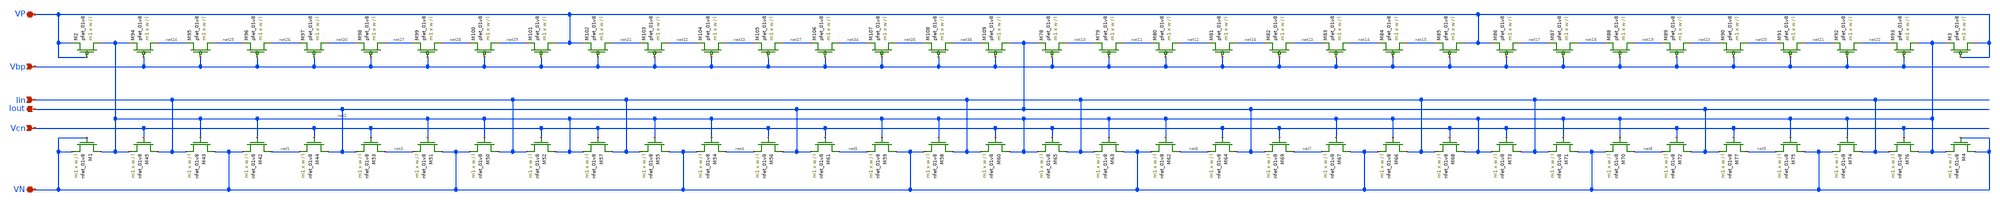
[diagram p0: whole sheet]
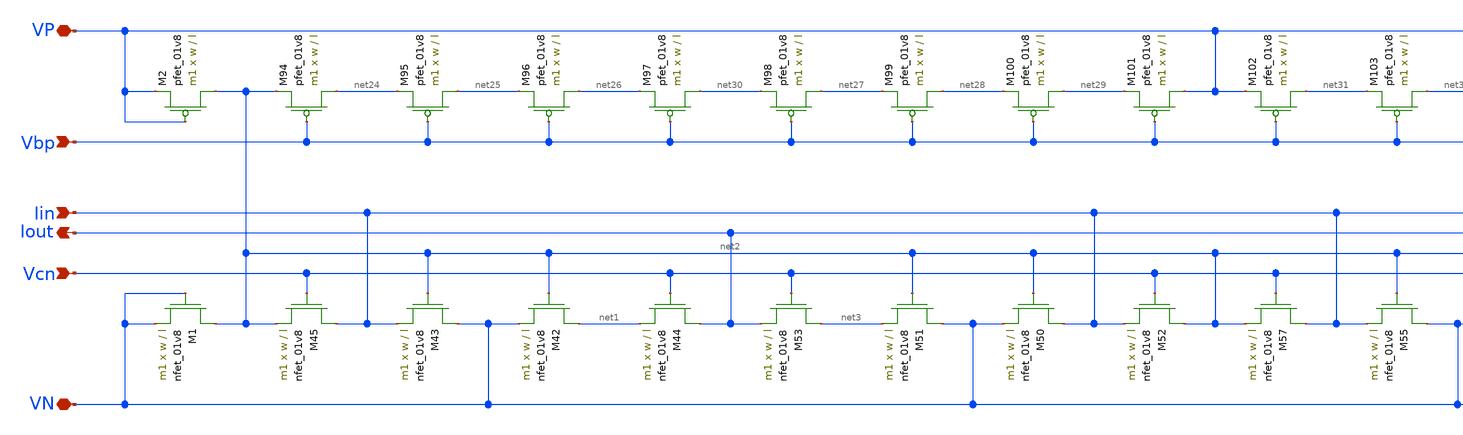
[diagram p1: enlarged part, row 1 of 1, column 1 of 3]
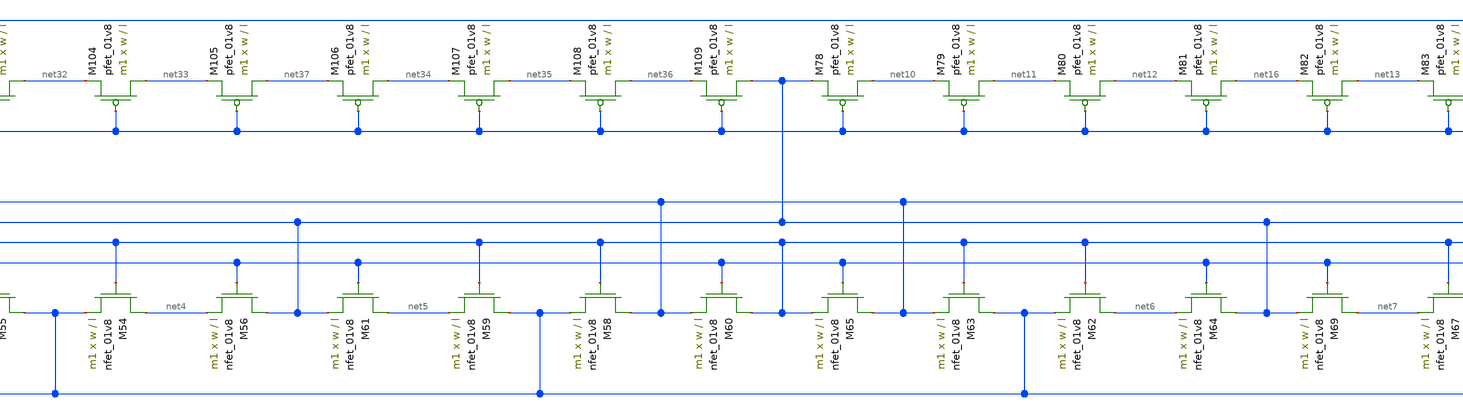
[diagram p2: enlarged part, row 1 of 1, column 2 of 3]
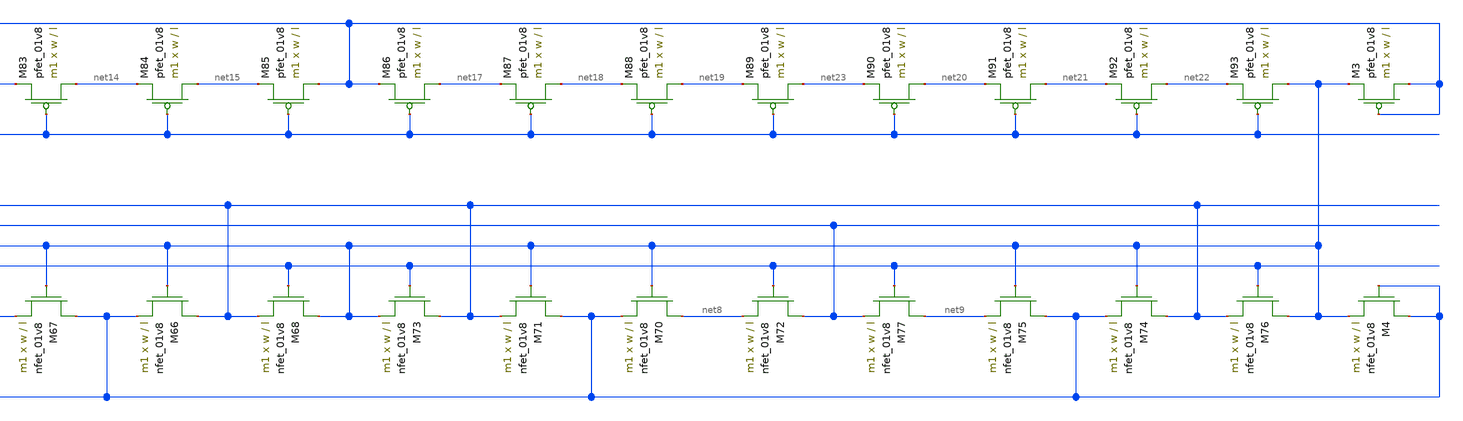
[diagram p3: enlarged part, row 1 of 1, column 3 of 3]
** sch_path: schematic/old/iout_mirror_LDS.sch
**.subckt iout_mirror_LDS Vcn Vbp Iout Iin VN VP
*.ipin Vcn
*.ipin Vbp
*.opin Iout
*.ipin Iin
*.iopin VN
*.iopin VP
XM42 net1 net2 VN GND sky130_fd_pr__nfet_01v8 L=l W=w nf=1 ad='int((nf+1)/2) * W/nf * 0.29' as='int((nf+2)/2) * W/nf * 0.29'
+ pd='2*int((nf+1)/2) * (W/nf + 0.29)' ps='2*int((nf+2)/2) * (W/nf + 0.29)' nrd='0.29 / W' nrs='0.29 / W'
+ sa=0 sb=0 sd=0 mult=m1 m=m1
XM43 VN net2 Iin GND sky130_fd_pr__nfet_01v8 L=l W=w nf=1 ad='int((nf+1)/2) * W/nf * 0.29' as='int((nf+2)/2) * W/nf * 0.29'
+ pd='2*int((nf+1)/2) * (W/nf + 0.29)' ps='2*int((nf+2)/2) * (W/nf + 0.29)' nrd='0.29 / W' nrs='0.29 / W'
+ sa=0 sb=0 sd=0 mult=m1 m=m1
XM44 Iout Vcn net1 GND sky130_fd_pr__nfet_01v8 L=l W=w nf=1 ad='int((nf+1)/2) * W/nf * 0.29' as='int((nf+2)/2) * W/nf * 0.29'
+ pd='2*int((nf+1)/2) * (W/nf + 0.29)' ps='2*int((nf+2)/2) * (W/nf + 0.29)' nrd='0.29 / W' nrs='0.29 / W'
+ sa=0 sb=0 sd=0 mult=m1 m=m1
XM45 Iin Vcn net2 GND sky130_fd_pr__nfet_01v8 L=l W=w nf=1 ad='int((nf+1)/2) * W/nf * 0.29' as='int((nf+2)/2) * W/nf * 0.29'
+ pd='2*int((nf+1)/2) * (W/nf + 0.29)' ps='2*int((nf+2)/2) * (W/nf + 0.29)' nrd='0.29 / W' nrs='0.29 / W'
+ sa=0 sb=0 sd=0 mult=m1 m=m1
XM50 Iin net2 VN GND sky130_fd_pr__nfet_01v8 L=l W=w nf=1 ad='int((nf+1)/2) * W/nf * 0.29' as='int((nf+2)/2) * W/nf * 0.29'
+ pd='2*int((nf+1)/2) * (W/nf + 0.29)' ps='2*int((nf+2)/2) * (W/nf + 0.29)' nrd='0.29 / W' nrs='0.29 / W'
+ sa=0 sb=0 sd=0 mult=m1 m=m1
XM51 VN net2 net3 GND sky130_fd_pr__nfet_01v8 L=l W=w nf=1 ad='int((nf+1)/2) * W/nf * 0.29' as='int((nf+2)/2) * W/nf * 0.29'
+ pd='2*int((nf+1)/2) * (W/nf + 0.29)' ps='2*int((nf+2)/2) * (W/nf + 0.29)' nrd='0.29 / W' nrs='0.29 / W'
+ sa=0 sb=0 sd=0 mult=m1 m=m1
XM52 net2 Vcn Iin GND sky130_fd_pr__nfet_01v8 L=l W=w nf=1 ad='int((nf+1)/2) * W/nf * 0.29' as='int((nf+2)/2) * W/nf * 0.29'
+ pd='2*int((nf+1)/2) * (W/nf + 0.29)' ps='2*int((nf+2)/2) * (W/nf + 0.29)' nrd='0.29 / W' nrs='0.29 / W'
+ sa=0 sb=0 sd=0 mult=m1 m=m1
XM53 net3 Vcn Iout GND sky130_fd_pr__nfet_01v8 L=l W=w nf=1 ad='int((nf+1)/2) * W/nf * 0.29' as='int((nf+2)/2) * W/nf * 0.29'
+ pd='2*int((nf+1)/2) * (W/nf + 0.29)' ps='2*int((nf+2)/2) * (W/nf + 0.29)' nrd='0.29 / W' nrs='0.29 / W'
+ sa=0 sb=0 sd=0 mult=m1 m=m1
XM54 net4 net2 VN GND sky130_fd_pr__nfet_01v8 L=l W=w nf=1 ad='int((nf+1)/2) * W/nf * 0.29' as='int((nf+2)/2) * W/nf * 0.29'
+ pd='2*int((nf+1)/2) * (W/nf + 0.29)' ps='2*int((nf+2)/2) * (W/nf + 0.29)' nrd='0.29 / W' nrs='0.29 / W'
+ sa=0 sb=0 sd=0 mult=m1 m=m1
XM55 VN net2 Iin GND sky130_fd_pr__nfet_01v8 L=l W=w nf=1 ad='int((nf+1)/2) * W/nf * 0.29' as='int((nf+2)/2) * W/nf * 0.29'
+ pd='2*int((nf+1)/2) * (W/nf + 0.29)' ps='2*int((nf+2)/2) * (W/nf + 0.29)' nrd='0.29 / W' nrs='0.29 / W'
+ sa=0 sb=0 sd=0 mult=m1 m=m1
XM56 Iout Vcn net4 GND sky130_fd_pr__nfet_01v8 L=l W=w nf=1 ad='int((nf+1)/2) * W/nf * 0.29' as='int((nf+2)/2) * W/nf * 0.29'
+ pd='2*int((nf+1)/2) * (W/nf + 0.29)' ps='2*int((nf+2)/2) * (W/nf + 0.29)' nrd='0.29 / W' nrs='0.29 / W'
+ sa=0 sb=0 sd=0 mult=m1 m=m1
XM57 Iin Vcn net2 GND sky130_fd_pr__nfet_01v8 L=l W=w nf=1 ad='int((nf+1)/2) * W/nf * 0.29' as='int((nf+2)/2) * W/nf * 0.29'
+ pd='2*int((nf+1)/2) * (W/nf + 0.29)' ps='2*int((nf+2)/2) * (W/nf + 0.29)' nrd='0.29 / W' nrs='0.29 / W'
+ sa=0 sb=0 sd=0 mult=m1 m=m1
XM58 Iin net2 VN GND sky130_fd_pr__nfet_01v8 L=l W=w nf=1 ad='int((nf+1)/2) * W/nf * 0.29' as='int((nf+2)/2) * W/nf * 0.29'
+ pd='2*int((nf+1)/2) * (W/nf + 0.29)' ps='2*int((nf+2)/2) * (W/nf + 0.29)' nrd='0.29 / W' nrs='0.29 / W'
+ sa=0 sb=0 sd=0 mult=m1 m=m1
XM59 VN net2 net5 GND sky130_fd_pr__nfet_01v8 L=l W=w nf=1 ad='int((nf+1)/2) * W/nf * 0.29' as='int((nf+2)/2) * W/nf * 0.29'
+ pd='2*int((nf+1)/2) * (W/nf + 0.29)' ps='2*int((nf+2)/2) * (W/nf + 0.29)' nrd='0.29 / W' nrs='0.29 / W'
+ sa=0 sb=0 sd=0 mult=m1 m=m1
XM60 net2 Vcn Iin GND sky130_fd_pr__nfet_01v8 L=l W=w nf=1 ad='int((nf+1)/2) * W/nf * 0.29' as='int((nf+2)/2) * W/nf * 0.29'
+ pd='2*int((nf+1)/2) * (W/nf + 0.29)' ps='2*int((nf+2)/2) * (W/nf + 0.29)' nrd='0.29 / W' nrs='0.29 / W'
+ sa=0 sb=0 sd=0 mult=m1 m=m1
XM61 net5 Vcn Iout GND sky130_fd_pr__nfet_01v8 L=l W=w nf=1 ad='int((nf+1)/2) * W/nf * 0.29' as='int((nf+2)/2) * W/nf * 0.29'
+ pd='2*int((nf+1)/2) * (W/nf + 0.29)' ps='2*int((nf+2)/2) * (W/nf + 0.29)' nrd='0.29 / W' nrs='0.29 / W'
+ sa=0 sb=0 sd=0 mult=m1 m=m1
XM62 net6 net2 VN GND sky130_fd_pr__nfet_01v8 L=l W=w nf=1 ad='int((nf+1)/2) * W/nf * 0.29' as='int((nf+2)/2) * W/nf * 0.29'
+ pd='2*int((nf+1)/2) * (W/nf + 0.29)' ps='2*int((nf+2)/2) * (W/nf + 0.29)' nrd='0.29 / W' nrs='0.29 / W'
+ sa=0 sb=0 sd=0 mult=m1 m=m1
XM63 VN net2 Iin GND sky130_fd_pr__nfet_01v8 L=l W=w nf=1 ad='int((nf+1)/2) * W/nf * 0.29' as='int((nf+2)/2) * W/nf * 0.29'
+ pd='2*int((nf+1)/2) * (W/nf + 0.29)' ps='2*int((nf+2)/2) * (W/nf + 0.29)' nrd='0.29 / W' nrs='0.29 / W'
+ sa=0 sb=0 sd=0 mult=m1 m=m1
XM64 Iout Vcn net6 GND sky130_fd_pr__nfet_01v8 L=l W=w nf=1 ad='int((nf+1)/2) * W/nf * 0.29' as='int((nf+2)/2) * W/nf * 0.29'
+ pd='2*int((nf+1)/2) * (W/nf + 0.29)' ps='2*int((nf+2)/2) * (W/nf + 0.29)' nrd='0.29 / W' nrs='0.29 / W'
+ sa=0 sb=0 sd=0 mult=m1 m=m1
XM65 Iin Vcn net2 GND sky130_fd_pr__nfet_01v8 L=l W=w nf=1 ad='int((nf+1)/2) * W/nf * 0.29' as='int((nf+2)/2) * W/nf * 0.29'
+ pd='2*int((nf+1)/2) * (W/nf + 0.29)' ps='2*int((nf+2)/2) * (W/nf + 0.29)' nrd='0.29 / W' nrs='0.29 / W'
+ sa=0 sb=0 sd=0 mult=m1 m=m1
XM66 Iin net2 VN GND sky130_fd_pr__nfet_01v8 L=l W=w nf=1 ad='int((nf+1)/2) * W/nf * 0.29' as='int((nf+2)/2) * W/nf * 0.29'
+ pd='2*int((nf+1)/2) * (W/nf + 0.29)' ps='2*int((nf+2)/2) * (W/nf + 0.29)' nrd='0.29 / W' nrs='0.29 / W'
+ sa=0 sb=0 sd=0 mult=m1 m=m1
XM67 VN net2 net7 GND sky130_fd_pr__nfet_01v8 L=l W=w nf=1 ad='int((nf+1)/2) * W/nf * 0.29' as='int((nf+2)/2) * W/nf * 0.29'
+ pd='2*int((nf+1)/2) * (W/nf + 0.29)' ps='2*int((nf+2)/2) * (W/nf + 0.29)' nrd='0.29 / W' nrs='0.29 / W'
+ sa=0 sb=0 sd=0 mult=m1 m=m1
XM68 net2 Vcn Iin GND sky130_fd_pr__nfet_01v8 L=l W=w nf=1 ad='int((nf+1)/2) * W/nf * 0.29' as='int((nf+2)/2) * W/nf * 0.29'
+ pd='2*int((nf+1)/2) * (W/nf + 0.29)' ps='2*int((nf+2)/2) * (W/nf + 0.29)' nrd='0.29 / W' nrs='0.29 / W'
+ sa=0 sb=0 sd=0 mult=m1 m=m1
XM69 net7 Vcn Iout GND sky130_fd_pr__nfet_01v8 L=l W=w nf=1 ad='int((nf+1)/2) * W/nf * 0.29' as='int((nf+2)/2) * W/nf * 0.29'
+ pd='2*int((nf+1)/2) * (W/nf + 0.29)' ps='2*int((nf+2)/2) * (W/nf + 0.29)' nrd='0.29 / W' nrs='0.29 / W'
+ sa=0 sb=0 sd=0 mult=m1 m=m1
XM70 net8 net2 VN GND sky130_fd_pr__nfet_01v8 L=l W=w nf=1 ad='int((nf+1)/2) * W/nf * 0.29' as='int((nf+2)/2) * W/nf * 0.29'
+ pd='2*int((nf+1)/2) * (W/nf + 0.29)' ps='2*int((nf+2)/2) * (W/nf + 0.29)' nrd='0.29 / W' nrs='0.29 / W'
+ sa=0 sb=0 sd=0 mult=m1 m=m1
XM71 VN net2 Iin GND sky130_fd_pr__nfet_01v8 L=l W=w nf=1 ad='int((nf+1)/2) * W/nf * 0.29' as='int((nf+2)/2) * W/nf * 0.29'
+ pd='2*int((nf+1)/2) * (W/nf + 0.29)' ps='2*int((nf+2)/2) * (W/nf + 0.29)' nrd='0.29 / W' nrs='0.29 / W'
+ sa=0 sb=0 sd=0 mult=m1 m=m1
XM72 Iout Vcn net8 GND sky130_fd_pr__nfet_01v8 L=l W=w nf=1 ad='int((nf+1)/2) * W/nf * 0.29' as='int((nf+2)/2) * W/nf * 0.29'
+ pd='2*int((nf+1)/2) * (W/nf + 0.29)' ps='2*int((nf+2)/2) * (W/nf + 0.29)' nrd='0.29 / W' nrs='0.29 / W'
+ sa=0 sb=0 sd=0 mult=m1 m=m1
XM73 Iin Vcn net2 GND sky130_fd_pr__nfet_01v8 L=l W=w nf=1 ad='int((nf+1)/2) * W/nf * 0.29' as='int((nf+2)/2) * W/nf * 0.29'
+ pd='2*int((nf+1)/2) * (W/nf + 0.29)' ps='2*int((nf+2)/2) * (W/nf + 0.29)' nrd='0.29 / W' nrs='0.29 / W'
+ sa=0 sb=0 sd=0 mult=m1 m=m1
XM74 Iin net2 VN GND sky130_fd_pr__nfet_01v8 L=l W=w nf=1 ad='int((nf+1)/2) * W/nf * 0.29' as='int((nf+2)/2) * W/nf * 0.29'
+ pd='2*int((nf+1)/2) * (W/nf + 0.29)' ps='2*int((nf+2)/2) * (W/nf + 0.29)' nrd='0.29 / W' nrs='0.29 / W'
+ sa=0 sb=0 sd=0 mult=m1 m=m1
XM75 VN net2 net9 GND sky130_fd_pr__nfet_01v8 L=l W=w nf=1 ad='int((nf+1)/2) * W/nf * 0.29' as='int((nf+2)/2) * W/nf * 0.29'
+ pd='2*int((nf+1)/2) * (W/nf + 0.29)' ps='2*int((nf+2)/2) * (W/nf + 0.29)' nrd='0.29 / W' nrs='0.29 / W'
+ sa=0 sb=0 sd=0 mult=m1 m=m1
XM76 net2 Vcn Iin GND sky130_fd_pr__nfet_01v8 L=l W=w nf=1 ad='int((nf+1)/2) * W/nf * 0.29' as='int((nf+2)/2) * W/nf * 0.29'
+ pd='2*int((nf+1)/2) * (W/nf + 0.29)' ps='2*int((nf+2)/2) * (W/nf + 0.29)' nrd='0.29 / W' nrs='0.29 / W'
+ sa=0 sb=0 sd=0 mult=m1 m=m1
XM77 net9 Vcn Iout GND sky130_fd_pr__nfet_01v8 L=l W=w nf=1 ad='int((nf+1)/2) * W/nf * 0.29' as='int((nf+2)/2) * W/nf * 0.29'
+ pd='2*int((nf+1)/2) * (W/nf + 0.29)' ps='2*int((nf+2)/2) * (W/nf + 0.29)' nrd='0.29 / W' nrs='0.29 / W'
+ sa=0 sb=0 sd=0 mult=m1 m=m1
XM78 net10 Vbp Iout VDD sky130_fd_pr__pfet_01v8 L=l W=w nf=1 ad='int((nf+1)/2) * W/nf * 0.29' as='int((nf+2)/2) * W/nf * 0.29'
+ pd='2*int((nf+1)/2) * (W/nf + 0.29)' ps='2*int((nf+2)/2) * (W/nf + 0.29)' nrd='0.29 / W' nrs='0.29 / W'
+ sa=0 sb=0 sd=0 mult=m1 m=m1
XM79 net11 Vbp net10 VDD sky130_fd_pr__pfet_01v8 L=l W=w nf=1 ad='int((nf+1)/2) * W/nf * 0.29' as='int((nf+2)/2) * W/nf * 0.29'
+ pd='2*int((nf+1)/2) * (W/nf + 0.29)' ps='2*int((nf+2)/2) * (W/nf + 0.29)' nrd='0.29 / W' nrs='0.29 / W'
+ sa=0 sb=0 sd=0 mult=m1 m=m1
XM80 net12 Vbp net11 VDD sky130_fd_pr__pfet_01v8 L=l W=w nf=1 ad='int((nf+1)/2) * W/nf * 0.29' as='int((nf+2)/2) * W/nf * 0.29'
+ pd='2*int((nf+1)/2) * (W/nf + 0.29)' ps='2*int((nf+2)/2) * (W/nf + 0.29)' nrd='0.29 / W' nrs='0.29 / W'
+ sa=0 sb=0 sd=0 mult=m1 m=m1
XM81 net16 Vbp net12 VDD sky130_fd_pr__pfet_01v8 L=l W=w nf=1 ad='int((nf+1)/2) * W/nf * 0.29' as='int((nf+2)/2) * W/nf * 0.29'
+ pd='2*int((nf+1)/2) * (W/nf + 0.29)' ps='2*int((nf+2)/2) * (W/nf + 0.29)' nrd='0.29 / W' nrs='0.29 / W'
+ sa=0 sb=0 sd=0 mult=m1 m=m1
XM82 net13 Vbp net16 VDD sky130_fd_pr__pfet_01v8 L=l W=w nf=1 ad='int((nf+1)/2) * W/nf * 0.29' as='int((nf+2)/2) * W/nf * 0.29'
+ pd='2*int((nf+1)/2) * (W/nf + 0.29)' ps='2*int((nf+2)/2) * (W/nf + 0.29)' nrd='0.29 / W' nrs='0.29 / W'
+ sa=0 sb=0 sd=0 mult=m1 m=m1
XM83 net14 Vbp net13 VDD sky130_fd_pr__pfet_01v8 L=l W=w nf=1 ad='int((nf+1)/2) * W/nf * 0.29' as='int((nf+2)/2) * W/nf * 0.29'
+ pd='2*int((nf+1)/2) * (W/nf + 0.29)' ps='2*int((nf+2)/2) * (W/nf + 0.29)' nrd='0.29 / W' nrs='0.29 / W'
+ sa=0 sb=0 sd=0 mult=m1 m=m1
XM84 net15 Vbp net14 VDD sky130_fd_pr__pfet_01v8 L=l W=w nf=1 ad='int((nf+1)/2) * W/nf * 0.29' as='int((nf+2)/2) * W/nf * 0.29'
+ pd='2*int((nf+1)/2) * (W/nf + 0.29)' ps='2*int((nf+2)/2) * (W/nf + 0.29)' nrd='0.29 / W' nrs='0.29 / W'
+ sa=0 sb=0 sd=0 mult=m1 m=m1
XM85 VP Vbp net15 VDD sky130_fd_pr__pfet_01v8 L=l W=w nf=1 ad='int((nf+1)/2) * W/nf * 0.29' as='int((nf+2)/2) * W/nf * 0.29'
+ pd='2*int((nf+1)/2) * (W/nf + 0.29)' ps='2*int((nf+2)/2) * (W/nf + 0.29)' nrd='0.29 / W' nrs='0.29 / W'
+ sa=0 sb=0 sd=0 mult=m1 m=m1
XM86 net17 Vbp VP VDD sky130_fd_pr__pfet_01v8 L=l W=w nf=1 ad='int((nf+1)/2) * W/nf * 0.29' as='int((nf+2)/2) * W/nf * 0.29'
+ pd='2*int((nf+1)/2) * (W/nf + 0.29)' ps='2*int((nf+2)/2) * (W/nf + 0.29)' nrd='0.29 / W' nrs='0.29 / W'
+ sa=0 sb=0 sd=0 mult=m1 m=m1
XM87 net18 Vbp net17 VDD sky130_fd_pr__pfet_01v8 L=l W=w nf=1 ad='int((nf+1)/2) * W/nf * 0.29' as='int((nf+2)/2) * W/nf * 0.29'
+ pd='2*int((nf+1)/2) * (W/nf + 0.29)' ps='2*int((nf+2)/2) * (W/nf + 0.29)' nrd='0.29 / W' nrs='0.29 / W'
+ sa=0 sb=0 sd=0 mult=m1 m=m1
XM88 net19 Vbp net18 VDD sky130_fd_pr__pfet_01v8 L=l W=w nf=1 ad='int((nf+1)/2) * W/nf * 0.29' as='int((nf+2)/2) * W/nf * 0.29'
+ pd='2*int((nf+1)/2) * (W/nf + 0.29)' ps='2*int((nf+2)/2) * (W/nf + 0.29)' nrd='0.29 / W' nrs='0.29 / W'
+ sa=0 sb=0 sd=0 mult=m1 m=m1
XM89 net23 Vbp net19 VDD sky130_fd_pr__pfet_01v8 L=l W=w nf=1 ad='int((nf+1)/2) * W/nf * 0.29' as='int((nf+2)/2) * W/nf * 0.29'
+ pd='2*int((nf+1)/2) * (W/nf + 0.29)' ps='2*int((nf+2)/2) * (W/nf + 0.29)' nrd='0.29 / W' nrs='0.29 / W'
+ sa=0 sb=0 sd=0 mult=m1 m=m1
XM90 net20 Vbp net23 VDD sky130_fd_pr__pfet_01v8 L=l W=w nf=1 ad='int((nf+1)/2) * W/nf * 0.29' as='int((nf+2)/2) * W/nf * 0.29'
+ pd='2*int((nf+1)/2) * (W/nf + 0.29)' ps='2*int((nf+2)/2) * (W/nf + 0.29)' nrd='0.29 / W' nrs='0.29 / W'
+ sa=0 sb=0 sd=0 mult=m1 m=m1
XM91 net21 Vbp net20 VDD sky130_fd_pr__pfet_01v8 L=l W=w nf=1 ad='int((nf+1)/2) * W/nf * 0.29' as='int((nf+2)/2) * W/nf * 0.29'
+ pd='2*int((nf+1)/2) * (W/nf + 0.29)' ps='2*int((nf+2)/2) * (W/nf + 0.29)' nrd='0.29 / W' nrs='0.29 / W'
+ sa=0 sb=0 sd=0 mult=m1 m=m1
XM92 net22 Vbp net21 VDD sky130_fd_pr__pfet_01v8 L=l W=w nf=1 ad='int((nf+1)/2) * W/nf * 0.29' as='int((nf+2)/2) * W/nf * 0.29'
+ pd='2*int((nf+1)/2) * (W/nf + 0.29)' ps='2*int((nf+2)/2) * (W/nf + 0.29)' nrd='0.29 / W' nrs='0.29 / W'
+ sa=0 sb=0 sd=0 mult=m1 m=m1
XM93 net2 Vbp net22 VDD sky130_fd_pr__pfet_01v8 L=l W=w nf=1 ad='int((nf+1)/2) * W/nf * 0.29' as='int((nf+2)/2) * W/nf * 0.29'
+ pd='2*int((nf+1)/2) * (W/nf + 0.29)' ps='2*int((nf+2)/2) * (W/nf + 0.29)' nrd='0.29 / W' nrs='0.29 / W'
+ sa=0 sb=0 sd=0 mult=m1 m=m1
XM94 net24 Vbp net2 VDD sky130_fd_pr__pfet_01v8 L=l W=w nf=1 ad='int((nf+1)/2) * W/nf * 0.29' as='int((nf+2)/2) * W/nf * 0.29'
+ pd='2*int((nf+1)/2) * (W/nf + 0.29)' ps='2*int((nf+2)/2) * (W/nf + 0.29)' nrd='0.29 / W' nrs='0.29 / W'
+ sa=0 sb=0 sd=0 mult=m1 m=m1
XM95 net25 Vbp net24 VDD sky130_fd_pr__pfet_01v8 L=l W=w nf=1 ad='int((nf+1)/2) * W/nf * 0.29' as='int((nf+2)/2) * W/nf * 0.29'
+ pd='2*int((nf+1)/2) * (W/nf + 0.29)' ps='2*int((nf+2)/2) * (W/nf + 0.29)' nrd='0.29 / W' nrs='0.29 / W'
+ sa=0 sb=0 sd=0 mult=m1 m=m1
XM96 net26 Vbp net25 VDD sky130_fd_pr__pfet_01v8 L=l W=w nf=1 ad='int((nf+1)/2) * W/nf * 0.29' as='int((nf+2)/2) * W/nf * 0.29'
+ pd='2*int((nf+1)/2) * (W/nf + 0.29)' ps='2*int((nf+2)/2) * (W/nf + 0.29)' nrd='0.29 / W' nrs='0.29 / W'
+ sa=0 sb=0 sd=0 mult=m1 m=m1
XM97 net30 Vbp net26 VDD sky130_fd_pr__pfet_01v8 L=l W=w nf=1 ad='int((nf+1)/2) * W/nf * 0.29' as='int((nf+2)/2) * W/nf * 0.29'
+ pd='2*int((nf+1)/2) * (W/nf + 0.29)' ps='2*int((nf+2)/2) * (W/nf + 0.29)' nrd='0.29 / W' nrs='0.29 / W'
+ sa=0 sb=0 sd=0 mult=m1 m=m1
XM98 net27 Vbp net30 VDD sky130_fd_pr__pfet_01v8 L=l W=w nf=1 ad='int((nf+1)/2) * W/nf * 0.29' as='int((nf+2)/2) * W/nf * 0.29'
+ pd='2*int((nf+1)/2) * (W/nf + 0.29)' ps='2*int((nf+2)/2) * (W/nf + 0.29)' nrd='0.29 / W' nrs='0.29 / W'
+ sa=0 sb=0 sd=0 mult=m1 m=m1
XM99 net28 Vbp net27 VDD sky130_fd_pr__pfet_01v8 L=l W=w nf=1 ad='int((nf+1)/2) * W/nf * 0.29' as='int((nf+2)/2) * W/nf * 0.29'
+ pd='2*int((nf+1)/2) * (W/nf + 0.29)' ps='2*int((nf+2)/2) * (W/nf + 0.29)' nrd='0.29 / W' nrs='0.29 / W'
+ sa=0 sb=0 sd=0 mult=m1 m=m1
XM100 net29 Vbp net28 VDD sky130_fd_pr__pfet_01v8 L=l W=w nf=1 ad='int((nf+1)/2) * W/nf * 0.29' as='int((nf+2)/2) * W/nf * 0.29'
+ pd='2*int((nf+1)/2) * (W/nf + 0.29)' ps='2*int((nf+2)/2) * (W/nf + 0.29)' nrd='0.29 / W' nrs='0.29 / W'
+ sa=0 sb=0 sd=0 mult=m1 m=m1
XM101 VP Vbp net29 VDD sky130_fd_pr__pfet_01v8 L=l W=w nf=1 ad='int((nf+1)/2) * W/nf * 0.29' as='int((nf+2)/2) * W/nf * 0.29'
+ pd='2*int((nf+1)/2) * (W/nf + 0.29)' ps='2*int((nf+2)/2) * (W/nf + 0.29)' nrd='0.29 / W' nrs='0.29 / W'
+ sa=0 sb=0 sd=0 mult=m1 m=m1
XM102 net31 Vbp VP VDD sky130_fd_pr__pfet_01v8 L=l W=w nf=1 ad='int((nf+1)/2) * W/nf * 0.29' as='int((nf+2)/2) * W/nf * 0.29'
+ pd='2*int((nf+1)/2) * (W/nf + 0.29)' ps='2*int((nf+2)/2) * (W/nf + 0.29)' nrd='0.29 / W' nrs='0.29 / W'
+ sa=0 sb=0 sd=0 mult=m1 m=m1
XM103 net32 Vbp net31 VDD sky130_fd_pr__pfet_01v8 L=l W=w nf=1 ad='int((nf+1)/2) * W/nf * 0.29' as='int((nf+2)/2) * W/nf * 0.29'
+ pd='2*int((nf+1)/2) * (W/nf + 0.29)' ps='2*int((nf+2)/2) * (W/nf + 0.29)' nrd='0.29 / W' nrs='0.29 / W'
+ sa=0 sb=0 sd=0 mult=m1 m=m1
XM104 net33 Vbp net32 VDD sky130_fd_pr__pfet_01v8 L=l W=w nf=1 ad='int((nf+1)/2) * W/nf * 0.29' as='int((nf+2)/2) * W/nf * 0.29'
+ pd='2*int((nf+1)/2) * (W/nf + 0.29)' ps='2*int((nf+2)/2) * (W/nf + 0.29)' nrd='0.29 / W' nrs='0.29 / W'
+ sa=0 sb=0 sd=0 mult=m1 m=m1
XM105 net37 Vbp net33 VDD sky130_fd_pr__pfet_01v8 L=l W=w nf=1 ad='int((nf+1)/2) * W/nf * 0.29' as='int((nf+2)/2) * W/nf * 0.29'
+ pd='2*int((nf+1)/2) * (W/nf + 0.29)' ps='2*int((nf+2)/2) * (W/nf + 0.29)' nrd='0.29 / W' nrs='0.29 / W'
+ sa=0 sb=0 sd=0 mult=m1 m=m1
XM106 net34 Vbp net37 VDD sky130_fd_pr__pfet_01v8 L=l W=w nf=1 ad='int((nf+1)/2) * W/nf * 0.29' as='int((nf+2)/2) * W/nf * 0.29'
+ pd='2*int((nf+1)/2) * (W/nf + 0.29)' ps='2*int((nf+2)/2) * (W/nf + 0.29)' nrd='0.29 / W' nrs='0.29 / W'
+ sa=0 sb=0 sd=0 mult=m1 m=m1
XM107 net35 Vbp net34 VDD sky130_fd_pr__pfet_01v8 L=l W=w nf=1 ad='int((nf+1)/2) * W/nf * 0.29' as='int((nf+2)/2) * W/nf * 0.29'
+ pd='2*int((nf+1)/2) * (W/nf + 0.29)' ps='2*int((nf+2)/2) * (W/nf + 0.29)' nrd='0.29 / W' nrs='0.29 / W'
+ sa=0 sb=0 sd=0 mult=m1 m=m1
XM108 net36 Vbp net35 VDD sky130_fd_pr__pfet_01v8 L=l W=w nf=1 ad='int((nf+1)/2) * W/nf * 0.29' as='int((nf+2)/2) * W/nf * 0.29'
+ pd='2*int((nf+1)/2) * (W/nf + 0.29)' ps='2*int((nf+2)/2) * (W/nf + 0.29)' nrd='0.29 / W' nrs='0.29 / W'
+ sa=0 sb=0 sd=0 mult=m1 m=m1
XM109 Iout Vbp net36 VDD sky130_fd_pr__pfet_01v8 L=l W=w nf=1 ad='int((nf+1)/2) * W/nf * 0.29' as='int((nf+2)/2) * W/nf * 0.29'
+ pd='2*int((nf+1)/2) * (W/nf + 0.29)' ps='2*int((nf+2)/2) * (W/nf + 0.29)' nrd='0.29 / W' nrs='0.29 / W'
+ sa=0 sb=0 sd=0 mult=m1 m=m1
XM1 net2 VN VN GND sky130_fd_pr__nfet_01v8 L=l W=w nf=1 ad='int((nf+1)/2) * W/nf * 0.29' as='int((nf+2)/2) * W/nf * 0.29'
+ pd='2*int((nf+1)/2) * (W/nf + 0.29)' ps='2*int((nf+2)/2) * (W/nf + 0.29)' nrd='0.29 / W' nrs='0.29 / W'
+ sa=0 sb=0 sd=0 mult=m1 m=m1
XM2 net2 VP VP VDD sky130_fd_pr__pfet_01v8 L=l W=w nf=1 ad='int((nf+1)/2) * W/nf * 0.29' as='int((nf+2)/2) * W/nf * 0.29'
+ pd='2*int((nf+1)/2) * (W/nf + 0.29)' ps='2*int((nf+2)/2) * (W/nf + 0.29)' nrd='0.29 / W' nrs='0.29 / W'
+ sa=0 sb=0 sd=0 mult=m1 m=m1
XM3 VP VP net2 VDD sky130_fd_pr__pfet_01v8 L=l W=w nf=1 ad='int((nf+1)/2) * W/nf * 0.29' as='int((nf+2)/2) * W/nf * 0.29'
+ pd='2*int((nf+1)/2) * (W/nf + 0.29)' ps='2*int((nf+2)/2) * (W/nf + 0.29)' nrd='0.29 / W' nrs='0.29 / W'
+ sa=0 sb=0 sd=0 mult=m1 m=m1
XM4 VN VN net2 GND sky130_fd_pr__nfet_01v8 L=l W=w nf=1 ad='int((nf+1)/2) * W/nf * 0.29' as='int((nf+2)/2) * W/nf * 0.29'
+ pd='2*int((nf+1)/2) * (W/nf + 0.29)' ps='2*int((nf+2)/2) * (W/nf + 0.29)' nrd='0.29 / W' nrs='0.29 / W'
+ sa=0 sb=0 sd=0 mult=m1 m=m1
**** begin user architecture code


.param w=5
.param l=2
.param m1=1


**** end user architecture code
**.ends
.end
